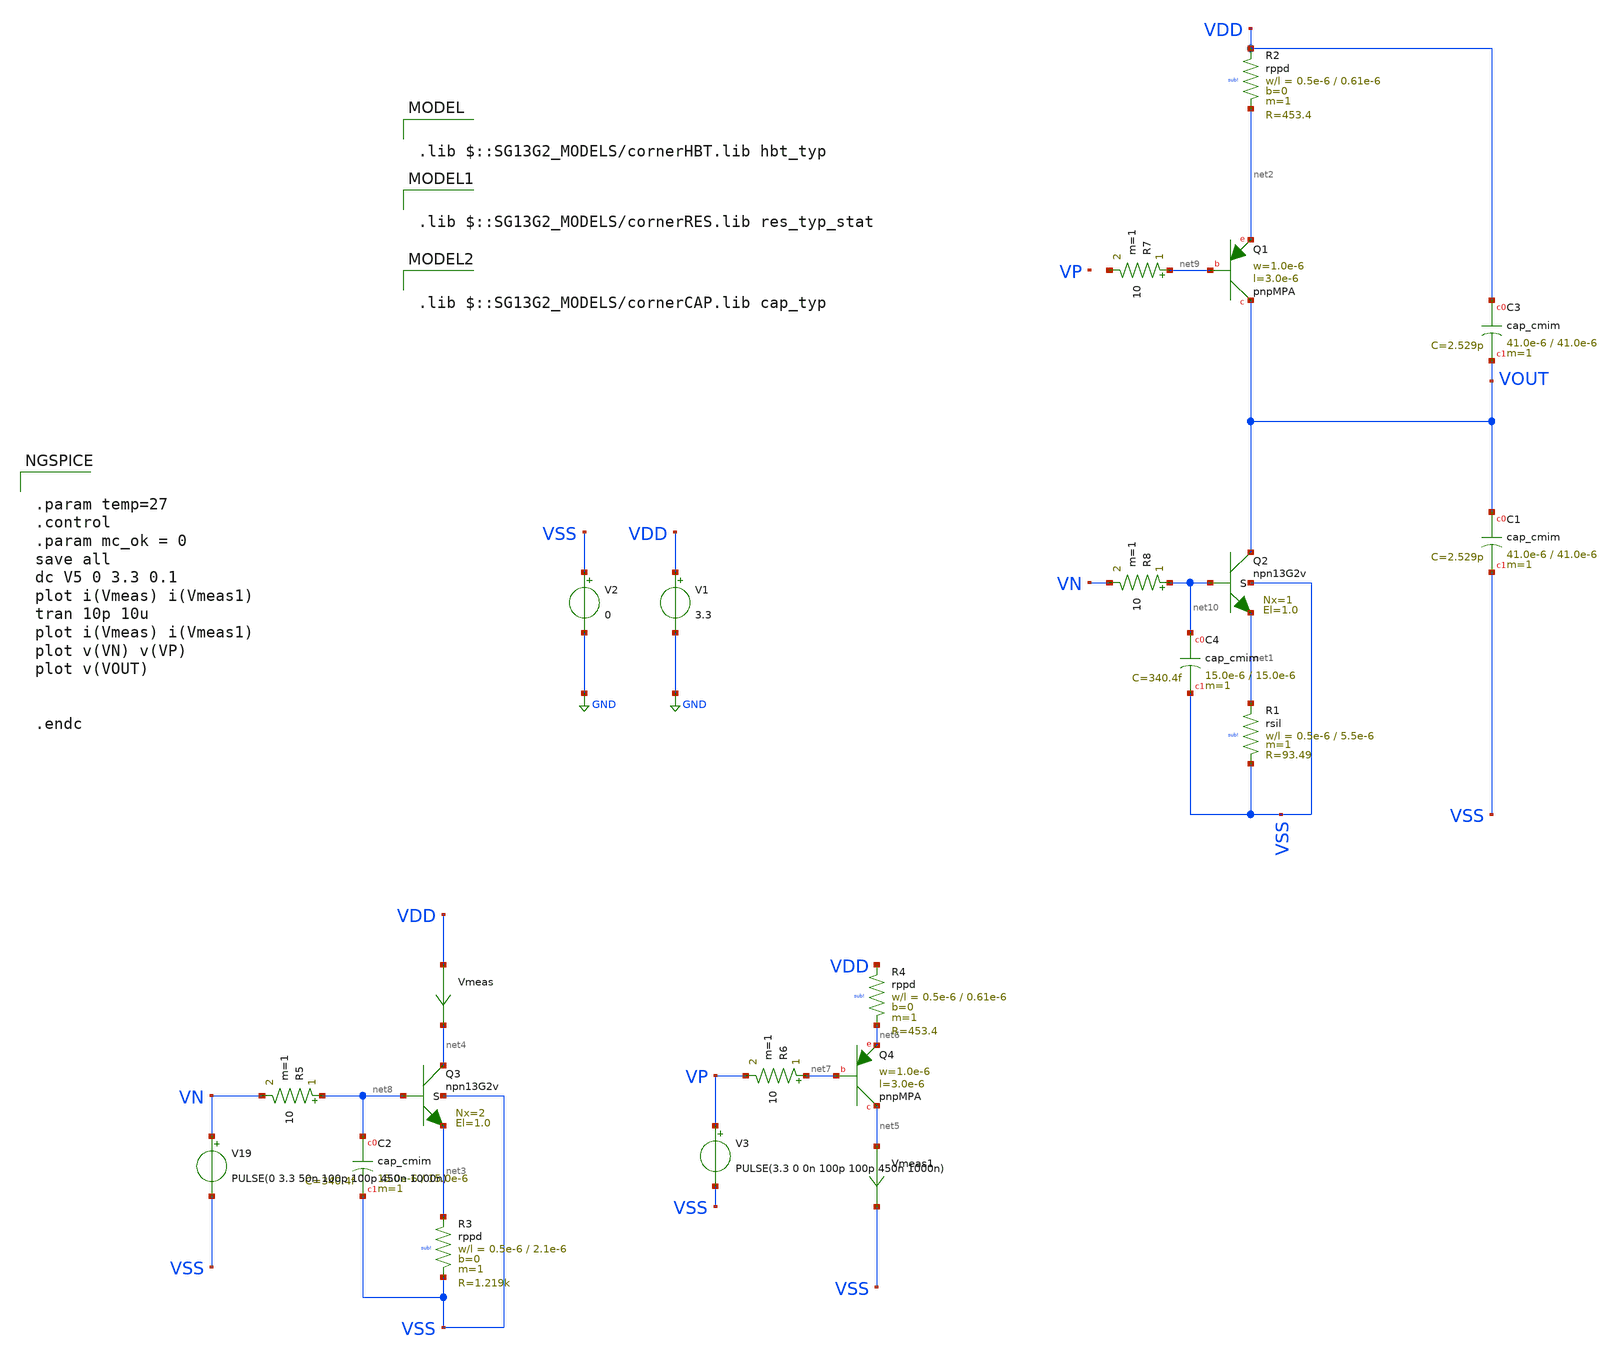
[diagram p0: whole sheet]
** sch_path: Learning/VCO/A_900_MHz_frequency_synthesizer_with_integrated_LC_voltage-controlled_oscillator_ihp130_3_3/testbench.sch
**.subckt testbench
XQ2 VOUT net10 net1 VSS npn13G2v Nx=1 El=1.0 mm_ok=1
V1 VDD GND 3.3
V2 VSS GND 0
XR1 net1 VSS sub! rsil w=0.5e-6 l=5.5e-6 m=1 mm_ok=1
XQ3 net4 net8 net3 VSS npn13G2v Nx=2 El=1.0 mm_ok=1
Vmeas VDD net4 0
.save i(vmeas)
XC3 VDD VOUT cap_cmim w=41.0e-6 l=41.0e-6 m=1 mm_ok=1
XC1 VOUT VSS cap_cmim w=41.0e-6 l=41.0e-6 m=1 mm_ok=1
XQ4 net5 net7 net6 pnpMPA a=3p p=8u m=4
Vmeas1 net5 VSS 0
.save i(vmeas1)
XR3 net3 VSS sub! rppd w=0.5e-6 l=2.1e-6 m=1 b=0 mm_ok=1
XR4 VDD net6 sub! rppd w=0.5e-6 l=0.61e-6 m=1 b=0 mm_ok=1
XQ1 VOUT net9 net2 pnpMPA a=3p p=8u m=4
XR2 VDD net2 sub! rppd w=0.5e-6 l=0.61e-6 m=1 b=0 mm_ok=1
XC2 net8 VSS cap_cmim w=15.0e-6 l=15.0e-6 m=1 mm_ok=1
R5 net8 VN 10 m=1
R6 net7 VP 10 m=1
V19 VN VSS PULSE(0 3.3 50n 100p 100p 450n 1000n)
V3 VP VSS PULSE(3.3 0 0n 100p 100p 450n 1000n)
R7 net9 net11 10 m=1
R8 net10 VN 10 m=1
XC4 net10 VSS cap_cmim w=15.0e-6 l=15.0e-6 m=1 mm_ok=1
**** begin user architecture code

.lib $::SG13G2_MODELS/cornerHBT.lib hbt_typ


.lib $::SG13G2_MODELS/cornerRES.lib res_typ_stat



.param temp=27
.control
.param mc_ok = 0
save all
dc V5 0 3.3 0.1
plot i(Vmeas) i(Vmeas1)
tran 10p 10u
plot i(Vmeas) i(Vmeas1)
plot v(VN) v(VP)
plot v(VOUT)


.endc



.lib $::SG13G2_MODELS/cornerCAP.lib cap_typ

**** end user architecture code
**.ends
.GLOBAL GND
.end
